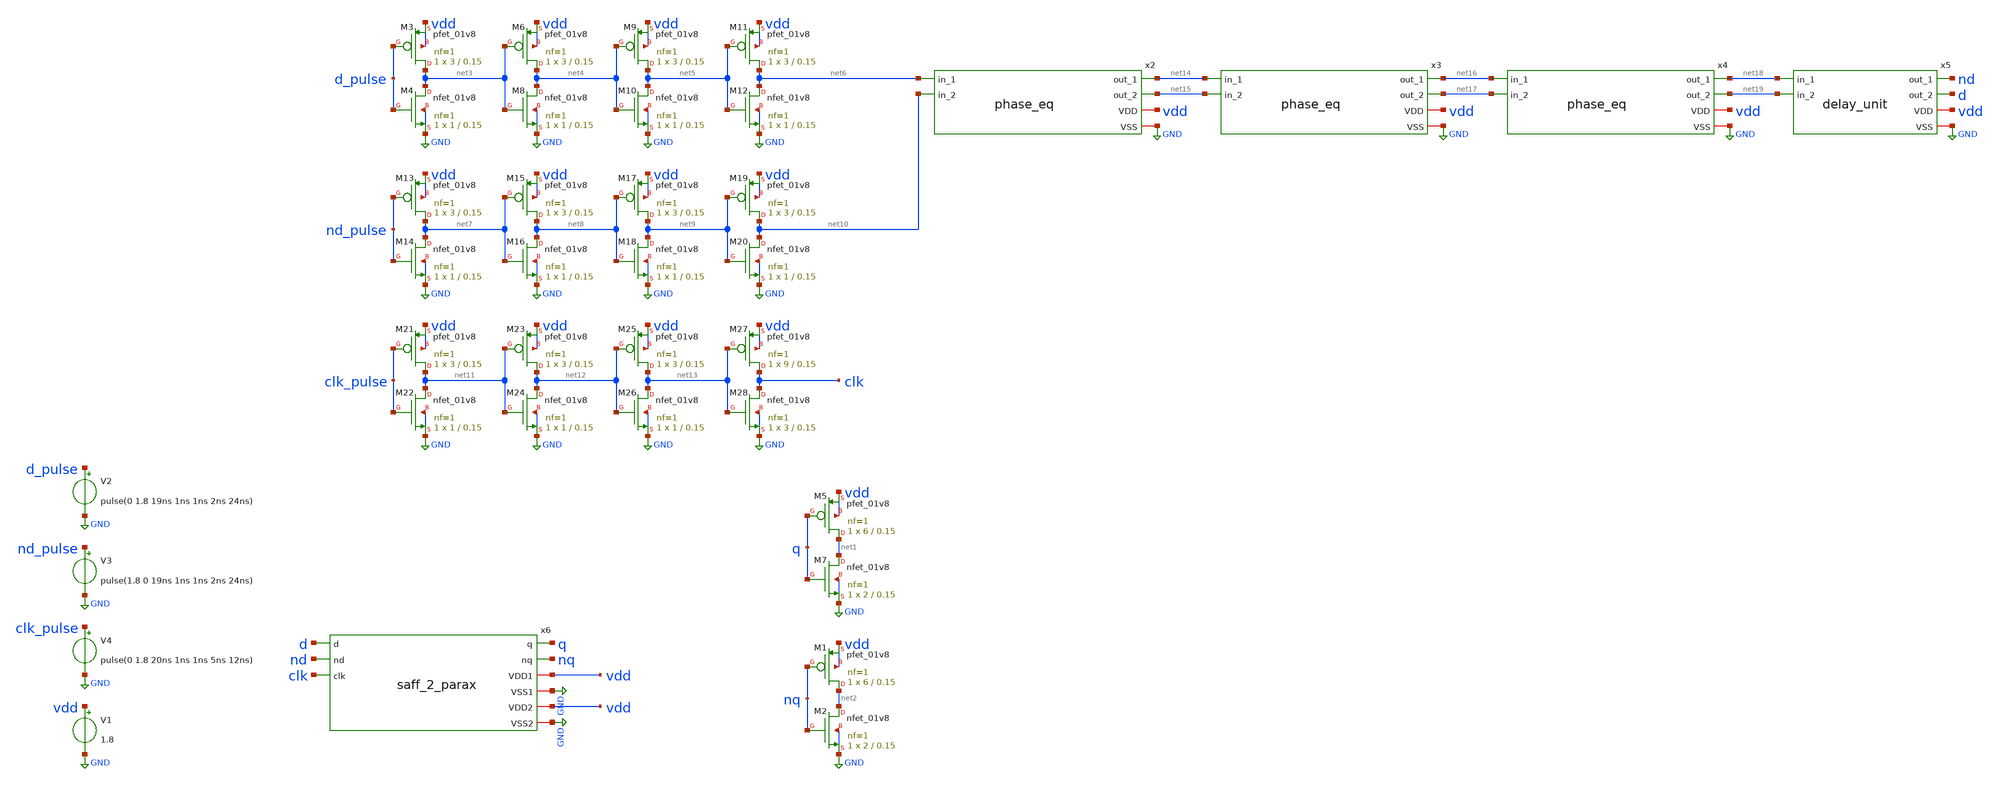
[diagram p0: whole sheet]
** sch_path: xschem/saff_2_tb_post_layout.sch
**.subckt saff_2_tb_post_layout
V1 vdd GND 1.8
V2 d_pulse GND pulse(0 1.8 19ns 1ns 1ns 2ns 24ns)
V3 nd_pulse GND pulse(1.8 0 19ns 1ns 1ns 2ns 24ns)
V4 clk_pulse GND pulse(0 1.8 20ns 1ns 1ns 5ns 12ns)
XM5 net1 q vdd vdd sky130_fd_pr__pfet_01v8 L=0.15 W=6 nf=1 ad='int((nf+1)/2) * W/nf * 0.29' as='int((nf+2)/2) * W/nf * 0.29'
+ pd='2*int((nf+1)/2) * (W/nf + 0.29)' ps='2*int((nf+2)/2) * (W/nf + 0.29)' nrd='0.29 / W' nrs='0.29 / W'
+ sa=0 sb=0 sd=0 mult=1 m=1
XM7 net1 q GND GND sky130_fd_pr__nfet_01v8 L=0.15 W=2 nf=1 ad='int((nf+1)/2) * W/nf * 0.29' as='int((nf+2)/2) * W/nf * 0.29'
+ pd='2*int((nf+1)/2) * (W/nf + 0.29)' ps='2*int((nf+2)/2) * (W/nf + 0.29)' nrd='0.29 / W' nrs='0.29 / W'
+ sa=0 sb=0 sd=0 mult=1 m=1
XM1 net2 nq vdd vdd sky130_fd_pr__pfet_01v8 L=0.15 W=6 nf=1 ad='int((nf+1)/2) * W/nf * 0.29' as='int((nf+2)/2) * W/nf * 0.29'
+ pd='2*int((nf+1)/2) * (W/nf + 0.29)' ps='2*int((nf+2)/2) * (W/nf + 0.29)' nrd='0.29 / W' nrs='0.29 / W'
+ sa=0 sb=0 sd=0 mult=1 m=1
XM2 net2 nq GND GND sky130_fd_pr__nfet_01v8 L=0.15 W=2 nf=1 ad='int((nf+1)/2) * W/nf * 0.29' as='int((nf+2)/2) * W/nf * 0.29'
+ pd='2*int((nf+1)/2) * (W/nf + 0.29)' ps='2*int((nf+2)/2) * (W/nf + 0.29)' nrd='0.29 / W' nrs='0.29 / W'
+ sa=0 sb=0 sd=0 mult=1 m=1
XM3 net3 d_pulse vdd vdd sky130_fd_pr__pfet_01v8 L=0.15 W=3 nf=1 ad='int((nf+1)/2) * W/nf * 0.29' as='int((nf+2)/2) * W/nf * 0.29'
+ pd='2*int((nf+1)/2) * (W/nf + 0.29)' ps='2*int((nf+2)/2) * (W/nf + 0.29)' nrd='0.29 / W' nrs='0.29 / W'
+ sa=0 sb=0 sd=0 mult=1 m=1
XM4 net3 d_pulse GND GND sky130_fd_pr__nfet_01v8 L=0.15 W=1 nf=1 ad='int((nf+1)/2) * W/nf * 0.29' as='int((nf+2)/2) * W/nf * 0.29'
+ pd='2*int((nf+1)/2) * (W/nf + 0.29)' ps='2*int((nf+2)/2) * (W/nf + 0.29)' nrd='0.29 / W' nrs='0.29 / W'
+ sa=0 sb=0 sd=0 mult=1 m=1
XM6 net4 net3 vdd vdd sky130_fd_pr__pfet_01v8 L=0.15 W=3 nf=1 ad='int((nf+1)/2) * W/nf * 0.29' as='int((nf+2)/2) * W/nf * 0.29'
+ pd='2*int((nf+1)/2) * (W/nf + 0.29)' ps='2*int((nf+2)/2) * (W/nf + 0.29)' nrd='0.29 / W' nrs='0.29 / W'
+ sa=0 sb=0 sd=0 mult=1 m=1
XM8 net4 net3 GND GND sky130_fd_pr__nfet_01v8 L=0.15 W=1 nf=1 ad='int((nf+1)/2) * W/nf * 0.29' as='int((nf+2)/2) * W/nf * 0.29'
+ pd='2*int((nf+1)/2) * (W/nf + 0.29)' ps='2*int((nf+2)/2) * (W/nf + 0.29)' nrd='0.29 / W' nrs='0.29 / W'
+ sa=0 sb=0 sd=0 mult=1 m=1
XM9 net5 net4 vdd vdd sky130_fd_pr__pfet_01v8 L=0.15 W=3 nf=1 ad='int((nf+1)/2) * W/nf * 0.29' as='int((nf+2)/2) * W/nf * 0.29'
+ pd='2*int((nf+1)/2) * (W/nf + 0.29)' ps='2*int((nf+2)/2) * (W/nf + 0.29)' nrd='0.29 / W' nrs='0.29 / W'
+ sa=0 sb=0 sd=0 mult=1 m=1
XM10 net5 net4 GND GND sky130_fd_pr__nfet_01v8 L=0.15 W=1 nf=1 ad='int((nf+1)/2) * W/nf * 0.29' as='int((nf+2)/2) * W/nf * 0.29'
+ pd='2*int((nf+1)/2) * (W/nf + 0.29)' ps='2*int((nf+2)/2) * (W/nf + 0.29)' nrd='0.29 / W' nrs='0.29 / W'
+ sa=0 sb=0 sd=0 mult=1 m=1
XM11 net6 net5 vdd vdd sky130_fd_pr__pfet_01v8 L=0.15 W=3 nf=1 ad='int((nf+1)/2) * W/nf * 0.29' as='int((nf+2)/2) * W/nf * 0.29'
+ pd='2*int((nf+1)/2) * (W/nf + 0.29)' ps='2*int((nf+2)/2) * (W/nf + 0.29)' nrd='0.29 / W' nrs='0.29 / W'
+ sa=0 sb=0 sd=0 mult=1 m=1
XM12 net6 net5 GND GND sky130_fd_pr__nfet_01v8 L=0.15 W=1 nf=1 ad='int((nf+1)/2) * W/nf * 0.29' as='int((nf+2)/2) * W/nf * 0.29'
+ pd='2*int((nf+1)/2) * (W/nf + 0.29)' ps='2*int((nf+2)/2) * (W/nf + 0.29)' nrd='0.29 / W' nrs='0.29 / W'
+ sa=0 sb=0 sd=0 mult=1 m=1
XM13 net7 nd_pulse vdd vdd sky130_fd_pr__pfet_01v8 L=0.15 W=3 nf=1 ad='int((nf+1)/2) * W/nf * 0.29' as='int((nf+2)/2) * W/nf * 0.29'
+ pd='2*int((nf+1)/2) * (W/nf + 0.29)' ps='2*int((nf+2)/2) * (W/nf + 0.29)' nrd='0.29 / W' nrs='0.29 / W'
+ sa=0 sb=0 sd=0 mult=1 m=1
XM14 net7 nd_pulse GND GND sky130_fd_pr__nfet_01v8 L=0.15 W=1 nf=1 ad='int((nf+1)/2) * W/nf * 0.29' as='int((nf+2)/2) * W/nf * 0.29'
+ pd='2*int((nf+1)/2) * (W/nf + 0.29)' ps='2*int((nf+2)/2) * (W/nf + 0.29)' nrd='0.29 / W' nrs='0.29 / W'
+ sa=0 sb=0 sd=0 mult=1 m=1
XM15 net8 net7 vdd vdd sky130_fd_pr__pfet_01v8 L=0.15 W=3 nf=1 ad='int((nf+1)/2) * W/nf * 0.29' as='int((nf+2)/2) * W/nf * 0.29'
+ pd='2*int((nf+1)/2) * (W/nf + 0.29)' ps='2*int((nf+2)/2) * (W/nf + 0.29)' nrd='0.29 / W' nrs='0.29 / W'
+ sa=0 sb=0 sd=0 mult=1 m=1
XM16 net8 net7 GND GND sky130_fd_pr__nfet_01v8 L=0.15 W=1 nf=1 ad='int((nf+1)/2) * W/nf * 0.29' as='int((nf+2)/2) * W/nf * 0.29'
+ pd='2*int((nf+1)/2) * (W/nf + 0.29)' ps='2*int((nf+2)/2) * (W/nf + 0.29)' nrd='0.29 / W' nrs='0.29 / W'
+ sa=0 sb=0 sd=0 mult=1 m=1
XM17 net9 net8 vdd vdd sky130_fd_pr__pfet_01v8 L=0.15 W=3 nf=1 ad='int((nf+1)/2) * W/nf * 0.29' as='int((nf+2)/2) * W/nf * 0.29'
+ pd='2*int((nf+1)/2) * (W/nf + 0.29)' ps='2*int((nf+2)/2) * (W/nf + 0.29)' nrd='0.29 / W' nrs='0.29 / W'
+ sa=0 sb=0 sd=0 mult=1 m=1
XM18 net9 net8 GND GND sky130_fd_pr__nfet_01v8 L=0.15 W=1 nf=1 ad='int((nf+1)/2) * W/nf * 0.29' as='int((nf+2)/2) * W/nf * 0.29'
+ pd='2*int((nf+1)/2) * (W/nf + 0.29)' ps='2*int((nf+2)/2) * (W/nf + 0.29)' nrd='0.29 / W' nrs='0.29 / W'
+ sa=0 sb=0 sd=0 mult=1 m=1
XM19 net10 net9 vdd vdd sky130_fd_pr__pfet_01v8 L=0.15 W=3 nf=1 ad='int((nf+1)/2) * W/nf * 0.29' as='int((nf+2)/2) * W/nf * 0.29'
+ pd='2*int((nf+1)/2) * (W/nf + 0.29)' ps='2*int((nf+2)/2) * (W/nf + 0.29)' nrd='0.29 / W' nrs='0.29 / W'
+ sa=0 sb=0 sd=0 mult=1 m=1
XM20 net10 net9 GND GND sky130_fd_pr__nfet_01v8 L=0.15 W=1 nf=1 ad='int((nf+1)/2) * W/nf * 0.29' as='int((nf+2)/2) * W/nf * 0.29'
+ pd='2*int((nf+1)/2) * (W/nf + 0.29)' ps='2*int((nf+2)/2) * (W/nf + 0.29)' nrd='0.29 / W' nrs='0.29 / W'
+ sa=0 sb=0 sd=0 mult=1 m=1
XM21 net11 clk_pulse vdd vdd sky130_fd_pr__pfet_01v8 L=0.15 W=3 nf=1 ad='int((nf+1)/2) * W/nf * 0.29'
+ as='int((nf+2)/2) * W/nf * 0.29' pd='2*int((nf+1)/2) * (W/nf + 0.29)' ps='2*int((nf+2)/2) * (W/nf + 0.29)'
+ nrd='0.29 / W' nrs='0.29 / W' sa=0 sb=0 sd=0 mult=1 m=1
XM22 net11 clk_pulse GND GND sky130_fd_pr__nfet_01v8 L=0.15 W=1 nf=1 ad='int((nf+1)/2) * W/nf * 0.29'
+ as='int((nf+2)/2) * W/nf * 0.29' pd='2*int((nf+1)/2) * (W/nf + 0.29)' ps='2*int((nf+2)/2) * (W/nf + 0.29)'
+ nrd='0.29 / W' nrs='0.29 / W' sa=0 sb=0 sd=0 mult=1 m=1
XM23 net12 net11 vdd vdd sky130_fd_pr__pfet_01v8 L=0.15 W=3 nf=1 ad='int((nf+1)/2) * W/nf * 0.29' as='int((nf+2)/2) * W/nf * 0.29'
+ pd='2*int((nf+1)/2) * (W/nf + 0.29)' ps='2*int((nf+2)/2) * (W/nf + 0.29)' nrd='0.29 / W' nrs='0.29 / W'
+ sa=0 sb=0 sd=0 mult=1 m=1
XM24 net12 net11 GND GND sky130_fd_pr__nfet_01v8 L=0.15 W=1 nf=1 ad='int((nf+1)/2) * W/nf * 0.29' as='int((nf+2)/2) * W/nf * 0.29'
+ pd='2*int((nf+1)/2) * (W/nf + 0.29)' ps='2*int((nf+2)/2) * (W/nf + 0.29)' nrd='0.29 / W' nrs='0.29 / W'
+ sa=0 sb=0 sd=0 mult=1 m=1
XM25 net13 net12 vdd vdd sky130_fd_pr__pfet_01v8 L=0.15 W=3 nf=1 ad='int((nf+1)/2) * W/nf * 0.29' as='int((nf+2)/2) * W/nf * 0.29'
+ pd='2*int((nf+1)/2) * (W/nf + 0.29)' ps='2*int((nf+2)/2) * (W/nf + 0.29)' nrd='0.29 / W' nrs='0.29 / W'
+ sa=0 sb=0 sd=0 mult=1 m=1
XM26 net13 net12 GND GND sky130_fd_pr__nfet_01v8 L=0.15 W=1 nf=1 ad='int((nf+1)/2) * W/nf * 0.29' as='int((nf+2)/2) * W/nf * 0.29'
+ pd='2*int((nf+1)/2) * (W/nf + 0.29)' ps='2*int((nf+2)/2) * (W/nf + 0.29)' nrd='0.29 / W' nrs='0.29 / W'
+ sa=0 sb=0 sd=0 mult=1 m=1
XM27 clk net13 vdd vdd sky130_fd_pr__pfet_01v8 L=0.15 W=9 nf=1 ad='int((nf+1)/2) * W/nf * 0.29' as='int((nf+2)/2) * W/nf * 0.29'
+ pd='2*int((nf+1)/2) * (W/nf + 0.29)' ps='2*int((nf+2)/2) * (W/nf + 0.29)' nrd='0.29 / W' nrs='0.29 / W'
+ sa=0 sb=0 sd=0 mult=1 m=1
XM28 clk net13 GND GND sky130_fd_pr__nfet_01v8 L=0.15 W=3 nf=1 ad='int((nf+1)/2) * W/nf * 0.29' as='int((nf+2)/2) * W/nf * 0.29'
+ pd='2*int((nf+1)/2) * (W/nf + 0.29)' ps='2*int((nf+2)/2) * (W/nf + 0.29)' nrd='0.29 / W' nrs='0.29 / W'
+ sa=0 sb=0 sd=0 mult=1 m=1
x2 net14 net6 net15 net10 vdd GND phase_eq
x3 net16 net14 net17 net15 vdd GND phase_eq
x4 net18 net16 net19 net17 vdd GND phase_eq
x5 nd net18 net19 vdd d GND delay_unit
x6 d nd clk q nq vdd GND vdd GND saff_2_parax
**** begin user architecture code

** opencircuitdesign pdks install
.lib $::SKYWATER_MODELS/sky130.lib.spice tt





.tran 0.001n 50n
.save v(d) v(nd) v(clk) v(q) v(nq)

.control
run
set wr_vecnames
wrdata saff_tb_post_layout.txt v(d) v(nd) v(clk) v(q) v(nq)
.endc


**** end user architecture code
**.ends

* expanding   symbol:  phase_eq.sym # of pins=6
** sym_path: xschem/phase_eq.sym
** sch_path: xschem/phase_eq.sch
.subckt phase_eq out_1 in_1 out_2 in_2 VDD VSS
*.iopin VDD
*.ipin in_1
*.opin out_1
*.iopin VSS
*.ipin in_2
*.opin out_2
XM5 out_1 in_1 VDD VDD sky130_fd_pr__pfet_01v8 L=0.15 W=9 nf=1 ad='int((nf+1)/2) * W/nf * 0.29' as='int((nf+2)/2) * W/nf * 0.29'
+ pd='2*int((nf+1)/2) * (W/nf + 0.29)' ps='2*int((nf+2)/2) * (W/nf + 0.29)' nrd='0.29 / W' nrs='0.29 / W'
+ sa=0 sb=0 sd=0 mult=1 m=1
XM7 out_1 in_1 VSS VSS sky130_fd_pr__nfet_01v8 L=0.15 W=3 nf=1 ad='int((nf+1)/2) * W/nf * 0.29' as='int((nf+2)/2) * W/nf * 0.29'
+ pd='2*int((nf+1)/2) * (W/nf + 0.29)' ps='2*int((nf+2)/2) * (W/nf + 0.29)' nrd='0.29 / W' nrs='0.29 / W'
+ sa=0 sb=0 sd=0 mult=1 m=1
XM1 out_2 in_2 VDD VDD sky130_fd_pr__pfet_01v8 L=0.15 W=9 nf=1 ad='int((nf+1)/2) * W/nf * 0.29' as='int((nf+2)/2) * W/nf * 0.29'
+ pd='2*int((nf+1)/2) * (W/nf + 0.29)' ps='2*int((nf+2)/2) * (W/nf + 0.29)' nrd='0.29 / W' nrs='0.29 / W'
+ sa=0 sb=0 sd=0 mult=1 m=1
XM2 out_2 in_2 VSS VSS sky130_fd_pr__nfet_01v8 L=0.15 W=3 nf=1 ad='int((nf+1)/2) * W/nf * 0.29' as='int((nf+2)/2) * W/nf * 0.29'
+ pd='2*int((nf+1)/2) * (W/nf + 0.29)' ps='2*int((nf+2)/2) * (W/nf + 0.29)' nrd='0.29 / W' nrs='0.29 / W'
+ sa=0 sb=0 sd=0 mult=1 m=1
XM3 in_1 in_2 VDD VDD sky130_fd_pr__pfet_01v8 L=0.15 W=3 nf=1 ad='int((nf+1)/2) * W/nf * 0.29' as='int((nf+2)/2) * W/nf * 0.29'
+ pd='2*int((nf+1)/2) * (W/nf + 0.29)' ps='2*int((nf+2)/2) * (W/nf + 0.29)' nrd='0.29 / W' nrs='0.29 / W'
+ sa=0 sb=0 sd=0 mult=1 m=1
XM4 in_1 in_2 VSS VSS sky130_fd_pr__nfet_01v8 L=0.15 W=1 nf=1 ad='int((nf+1)/2) * W/nf * 0.29' as='int((nf+2)/2) * W/nf * 0.29'
+ pd='2*int((nf+1)/2) * (W/nf + 0.29)' ps='2*int((nf+2)/2) * (W/nf + 0.29)' nrd='0.29 / W' nrs='0.29 / W'
+ sa=0 sb=0 sd=0 mult=1 m=1
XM6 in_2 in_1 VDD VDD sky130_fd_pr__pfet_01v8 L=0.15 W=3 nf=1 ad='int((nf+1)/2) * W/nf * 0.29' as='int((nf+2)/2) * W/nf * 0.29'
+ pd='2*int((nf+1)/2) * (W/nf + 0.29)' ps='2*int((nf+2)/2) * (W/nf + 0.29)' nrd='0.29 / W' nrs='0.29 / W'
+ sa=0 sb=0 sd=0 mult=1 m=1
XM8 in_2 in_1 VSS VSS sky130_fd_pr__nfet_01v8 L=0.15 W=1 nf=1 ad='int((nf+1)/2) * W/nf * 0.29' as='int((nf+2)/2) * W/nf * 0.29'
+ pd='2*int((nf+1)/2) * (W/nf + 0.29)' ps='2*int((nf+2)/2) * (W/nf + 0.29)' nrd='0.29 / W' nrs='0.29 / W'
+ sa=0 sb=0 sd=0 mult=1 m=1
.ends


* expanding   symbol:  delay_unit.sym # of pins=6
** sym_path: xschem/delay_unit.sym
** sch_path: xschem/delay_unit.sch
.subckt delay_unit out_1 in_1 in_2 VDD out_2 VSS
*.iopin VDD
*.ipin in_1
*.opin out_1
*.iopin VSS
*.ipin in_2
*.opin out_2
XM5 out_2 in_1 VDD VDD sky130_fd_pr__pfet_01v8 L=0.15 W=9 nf=1 ad='int((nf+1)/2) * W/nf * 0.29' as='int((nf+2)/2) * W/nf * 0.29'
+ pd='2*int((nf+1)/2) * (W/nf + 0.29)' ps='2*int((nf+2)/2) * (W/nf + 0.29)' nrd='0.29 / W' nrs='0.29 / W'
+ sa=0 sb=0 sd=0 mult=1 m=1
XM7 out_2 in_1 VSS VSS sky130_fd_pr__nfet_01v8 L=0.15 W=3 nf=1 ad='int((nf+1)/2) * W/nf * 0.29' as='int((nf+2)/2) * W/nf * 0.29'
+ pd='2*int((nf+1)/2) * (W/nf + 0.29)' ps='2*int((nf+2)/2) * (W/nf + 0.29)' nrd='0.29 / W' nrs='0.29 / W'
+ sa=0 sb=0 sd=0 mult=1 m=1
XM1 out_1 in_2 VDD VDD sky130_fd_pr__pfet_01v8 L=0.15 W=9 nf=1 ad='int((nf+1)/2) * W/nf * 0.29' as='int((nf+2)/2) * W/nf * 0.29'
+ pd='2*int((nf+1)/2) * (W/nf + 0.29)' ps='2*int((nf+2)/2) * (W/nf + 0.29)' nrd='0.29 / W' nrs='0.29 / W'
+ sa=0 sb=0 sd=0 mult=1 m=1
XM2 out_1 in_2 VSS VSS sky130_fd_pr__nfet_01v8 L=0.15 W=3 nf=1 ad='int((nf+1)/2) * W/nf * 0.29' as='int((nf+2)/2) * W/nf * 0.29'
+ pd='2*int((nf+1)/2) * (W/nf + 0.29)' ps='2*int((nf+2)/2) * (W/nf + 0.29)' nrd='0.29 / W' nrs='0.29 / W'
+ sa=0 sb=0 sd=0 mult=1 m=1
XM3 in_1 in_2 VDD VDD sky130_fd_pr__pfet_01v8 L=0.15 W=3 nf=1 ad='int((nf+1)/2) * W/nf * 0.29' as='int((nf+2)/2) * W/nf * 0.29'
+ pd='2*int((nf+1)/2) * (W/nf + 0.29)' ps='2*int((nf+2)/2) * (W/nf + 0.29)' nrd='0.29 / W' nrs='0.29 / W'
+ sa=0 sb=0 sd=0 mult=1 m=1
XM4 in_1 in_2 VSS VSS sky130_fd_pr__nfet_01v8 L=0.15 W=1 nf=1 ad='int((nf+1)/2) * W/nf * 0.29' as='int((nf+2)/2) * W/nf * 0.29'
+ pd='2*int((nf+1)/2) * (W/nf + 0.29)' ps='2*int((nf+2)/2) * (W/nf + 0.29)' nrd='0.29 / W' nrs='0.29 / W'
+ sa=0 sb=0 sd=0 mult=1 m=1
XM6 in_2 in_1 VDD VDD sky130_fd_pr__pfet_01v8 L=0.15 W=3 nf=1 ad='int((nf+1)/2) * W/nf * 0.29' as='int((nf+2)/2) * W/nf * 0.29'
+ pd='2*int((nf+1)/2) * (W/nf + 0.29)' ps='2*int((nf+2)/2) * (W/nf + 0.29)' nrd='0.29 / W' nrs='0.29 / W'
+ sa=0 sb=0 sd=0 mult=1 m=1
XM8 in_2 in_1 VSS VSS sky130_fd_pr__nfet_01v8 L=0.15 W=1 nf=1 ad='int((nf+1)/2) * W/nf * 0.29' as='int((nf+2)/2) * W/nf * 0.29'
+ pd='2*int((nf+1)/2) * (W/nf + 0.29)' ps='2*int((nf+2)/2) * (W/nf + 0.29)' nrd='0.29 / W' nrs='0.29 / W'
+ sa=0 sb=0 sd=0 mult=1 m=1
.ends


* expanding   symbol:  saff_2_parax.sym # of pins=9
** sym_path: xschem/saff_2.sym
.include [file normalize ../mag/saff_2.sim.spice]
.GLOBAL GND
.end
